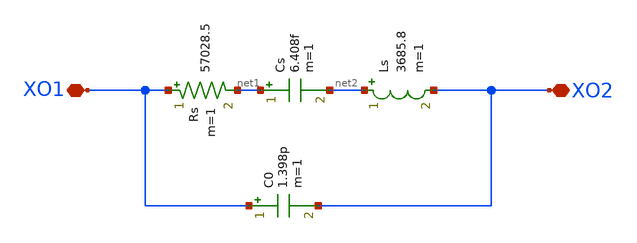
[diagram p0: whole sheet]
** sch_path: xtal_model.sch
**.subckt xtal_model XO2 XO1
*.iopin XO2
*.iopin XO1
Rs XO1 net1 57028.5 m=1
Cs net1 net2 6.408f m=1
C0 XO1 XO2 1.398p m=1
Ls net2 XO2 3685.8 m=1
**.ends
.end
